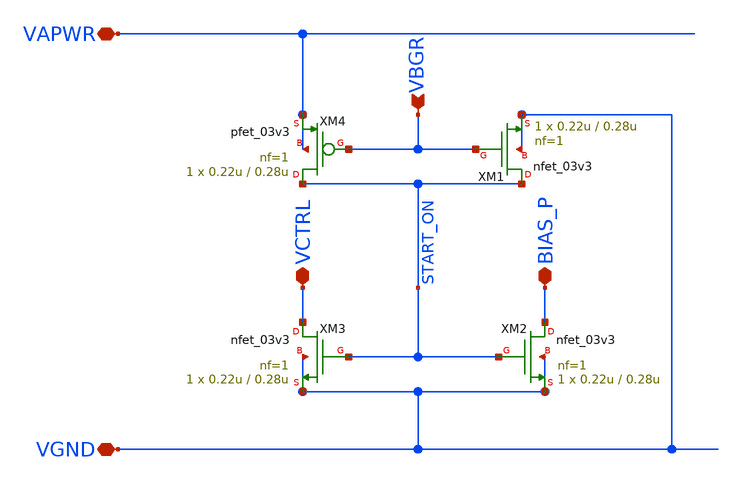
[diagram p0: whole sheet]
** sch_path: xschem/bgr_startup.sch
**.subckt bgr_startup VAPWR VGND VBGR BIAS_P VCTRL
*.iopin VAPWR
*.iopin VGND
*.ipin VBGR
*.iopin BIAS_P
*.iopin VCTRL
XM1 START_ON VBGR VGND VGND nfet_03v3 L=0.28u W=0.22u nf=1 ad='int((nf+1)/2) * W/nf * 0.18u' as='int((nf+2)/2) * W/nf * 0.18u'
+ pd='2*int((nf+1)/2) * (W/nf + 0.18u)' ps='2*int((nf+2)/2) * (W/nf + 0.18u)' nrd='0.18u / W' nrs='0.18u / W'
+ sa=0 sb=0 sd=0 m=1
XM2 BIAS_P START_ON VGND VGND nfet_03v3 L=0.28u W=0.22u nf=1 ad='int((nf+1)/2) * W/nf * 0.18u' as='int((nf+2)/2) * W/nf * 0.18u'
+ pd='2*int((nf+1)/2) * (W/nf + 0.18u)' ps='2*int((nf+2)/2) * (W/nf + 0.18u)' nrd='0.18u / W' nrs='0.18u / W'
+ sa=0 sb=0 sd=0 m=1
XM3 VCTRL START_ON VGND VGND nfet_03v3 L=0.28u W=0.22u nf=1 ad='int((nf+1)/2) * W/nf * 0.18u' as='int((nf+2)/2) * W/nf * 0.18u'
+ pd='2*int((nf+1)/2) * (W/nf + 0.18u)' ps='2*int((nf+2)/2) * (W/nf + 0.18u)' nrd='0.18u / W' nrs='0.18u / W'
+ sa=0 sb=0 sd=0 m=1
XM4 START_ON VBGR VAPWR VAPWR pfet_03v3 L=0.28u W=0.22u nf=1 ad='int((nf+1)/2) * W/nf * 0.18u' as='int((nf+2)/2) * W/nf * 0.18u'
+ pd='2*int((nf+1)/2) * (W/nf + 0.18u)' ps='2*int((nf+2)/2) * (W/nf + 0.18u)' nrd='0.18u / W' nrs='0.18u / W'
+ sa=0 sb=0 sd=0 m=1
**.ends
.end
